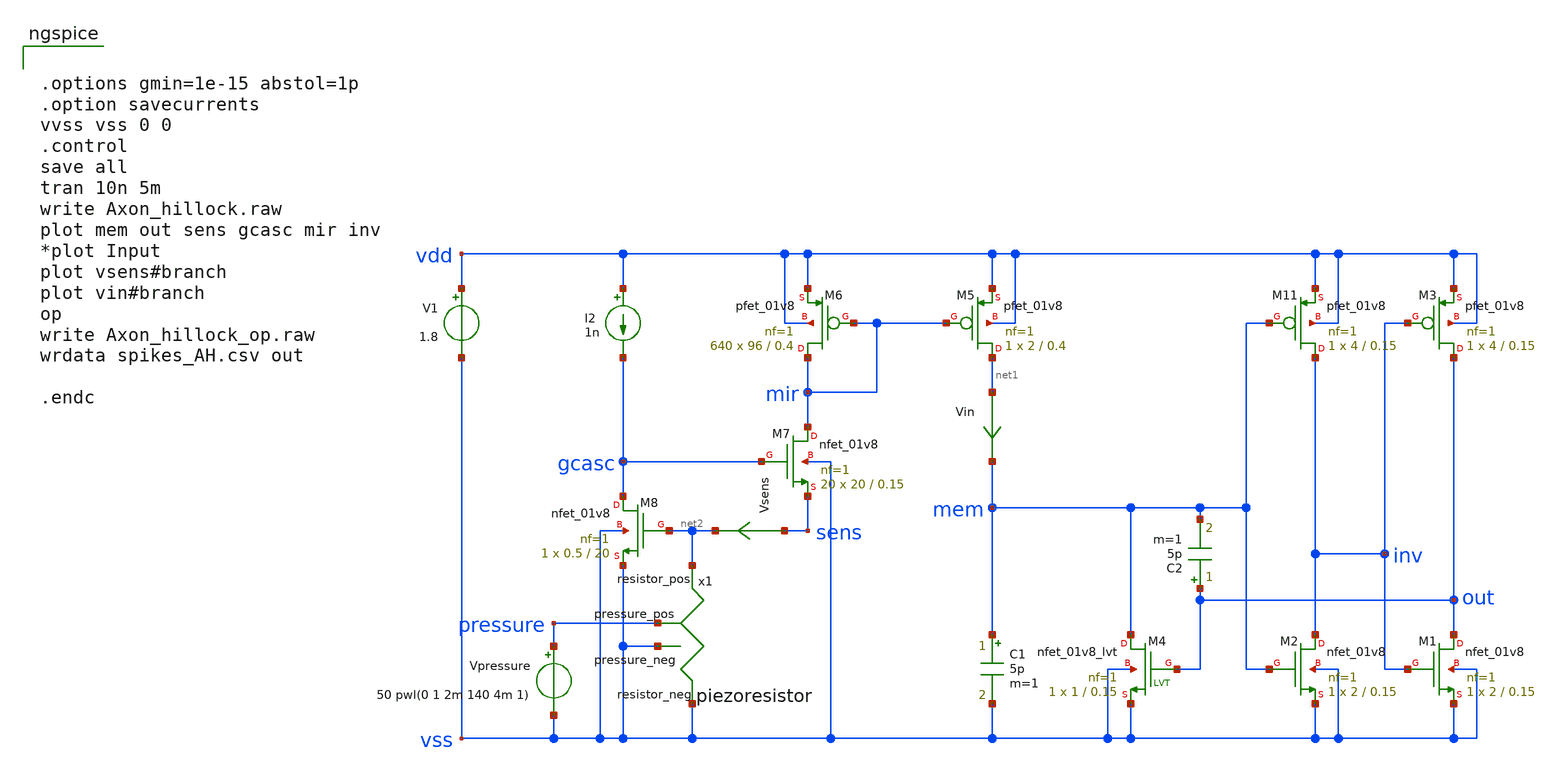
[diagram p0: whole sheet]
** sch_path: circuits/Axon_Hillock.sch
* Copyright 2020 Stefan Frederik Schippers
* Licensed under the Apache License, Version 2.0 (the "License");
* you may not use this file except in compliance with the License.
* You may obtain a copy of the License at
* https://www.apache.org/licenses/LICENSE-2.0
* Unless required by applicable law or agreed to in writing, software
* distributed under the License is distributed on an "AS IS" BASIS,
* WITHOUT WARRANTIES OR CONDITIONS OF ANY KIND, either express or implied.
* See the License for the specific language governing permissions and
* limitations under the License.
**.subckt Axon_Hillock
XM2 inv mem vss vss sky130_fd_pr__nfet_01v8 L=0.15 W=2 nf=1 ad='int((1 + 1)/2) * 2 / 1 * 0.29' as='int((1 + 2)/2) * 2 / 1 * 0.29'
+ pd='2*int((1 + 1)/2) * (2 / 1 + 0.29)' ps='2*int((1 + 2)/2) * (2 / 1 + 0.29)' nrd='0.29 / 2 ' nrs='0.29 / 2 '
+ sa=0 sb=0 sd=0 mult=1 m=1
XM11 inv mem vdd vdd sky130_fd_pr__pfet_01v8 L=0.15 W=4 nf=1 ad='int((nf+1)/2) * W/nf * 0.29' as='int((nf+2)/2) * W/nf * 0.29'
+ pd='2*int((nf+1)/2) * (W/nf + 0.29)' ps='2*int((nf+2)/2) * (W/nf + 0.29)' nrd='0.29 / W' nrs='0.29 / W'
+ sa=0 sb=0 sd=0 mult=1 m=1
XM1 out inv vss vss sky130_fd_pr__nfet_01v8 L=0.15 W=2 nf=1 ad='int((1 + 1)/2) * 2 / 1 * 0.29' as='int((1 + 2)/2) * 2 / 1 * 0.29'
+ pd='2*int((1 + 1)/2) * (2 / 1 + 0.29)' ps='2*int((1 + 2)/2) * (2 / 1 + 0.29)' nrd='0.29 / 2 ' nrs='0.29 / 2 '
+ sa=0 sb=0 sd=0 mult=1 m=1
XM3 out inv vdd vdd sky130_fd_pr__pfet_01v8 L=0.15 W=4 nf=1 ad='int((nf+1)/2) * W/nf * 0.29' as='int((nf+2)/2) * W/nf * 0.29'
+ pd='2*int((nf+1)/2) * (W/nf + 0.29)' ps='2*int((nf+2)/2) * (W/nf + 0.29)' nrd='0.29 / W' nrs='0.29 / W'
+ sa=0 sb=0 sd=0 mult=1 m=1
C2 out mem 5p m=1
V1 vdd vss 1.8
I2 vdd gcasc 1n
C1 mem vss 5p m=1
Vsens sens net2 0
.save i(vsens)
XM5 net1 mir vdd vdd sky130_fd_pr__pfet_01v8 L=0.4 W=2 nf=1 ad='int((nf+1)/2) * W/nf * 0.29' as='int((nf+2)/2) * W/nf * 0.29'
+ pd='2*int((nf+1)/2) * (W/nf + 0.29)' ps='2*int((nf+2)/2) * (W/nf + 0.29)' nrd='0.29 / W' nrs='0.29 / W'
+ sa=0 sb=0 sd=0 mult=1 m=1
XM6 mir mir vdd vdd sky130_fd_pr__pfet_01v8 L=0.4 W=96 nf=1 ad='int((nf+1)/2) * W/nf * 0.29' as='int((nf+2)/2) * W/nf * 0.29'
+ pd='2*int((nf+1)/2) * (W/nf + 0.29)' ps='2*int((nf+2)/2) * (W/nf + 0.29)' nrd='0.29 / W' nrs='0.29 / W'
+ sa=0 sb=0 sd=0 mult=640 m=640
XM4 mem out vss vss sky130_fd_pr__nfet_01v8_lvt L=0.15 W=1 nf=1 ad='int((1 + 1)/2) * 1 / 1 * 0.29' as='int((1 + 2)/2) * 1 / 1 * 0.29'
+ pd='2*int((1 + 1)/2) * (1 / 1 + 0.29)' ps='2*int((1 + 2)/2) * (1 / 1 + 0.29)' nrd='0.29 / 1 ' nrs='0.29 / 1 '
+ sa=0 sb=0 sd=0 mult=1 m=1
XM7 mir gcasc sens vss sky130_fd_pr__nfet_01v8 L=0.15 W=20 nf=1 ad='int((1 + 1)/2) * 20 / 1 * 0.29' as='int((1 + 2)/2) * 20 / 1 * 0.29'
+ pd='2*int((1 + 1)/2) * (20 / 1 + 0.29)' ps='2*int((1 + 2)/2) * (20 / 1 + 0.29)' nrd='0.29 / 20 ' nrs='0.29 / 20 '
+ sa=0 sb=0 sd=0 mult=20 m=20
XM8 gcasc net2 vss vss sky130_fd_pr__nfet_01v8 L=20 W=0.5 nf=1 ad='int((1 + 1)/2) * 0.5 / 1 * 0.29' as='int((1 + 2)/2) * 0.5 / 1 * 0.29'
+ pd='2*int((1 + 1)/2) * (0.5 / 1 + 0.29)' ps='2*int((1 + 2)/2) * (0.5 / 1 + 0.29)' nrd='0.29 / 0.5 ' nrs='0.29 / 0.5 '
+ sa=0 sb=0 sd=0 mult=1 m=1
Vin net1 mem 0
.save i(vin)
x1 pressure vss net2 vss piezoresistor
Vpressure pressure vss 50 pwl(0 1 2m 140 4m 1)
**** begin user architecture code


.options gmin=1e-15 abstol=1p
.option savecurrents
vvss vss 0 0
.control
save all
tran 10n 5m
write Axon_hillock.raw
plot mem out sens gcasc mir inv
*plot Input
plot vsens#branch
plot vin#branch
op
write Axon_hillock_op.raw
wrdata spikes_AH.csv out

.endc


 .lib $::SKYWATER_MODELS/models/sky130.lib.spice tt

.param mc_mm_switch=0
.param mc_pr_switch=1


**** end user architecture code
**.ends

* expanding   symbol:  /home/cmaier/.xschem/sky130_TAC3/circuits/piezoresistor.sym # of pins=4
** sym_path: circuits/piezoresistor.sym
** sch_path: circuits/piezoresistor.sch
.subckt piezoresistor pressure_pos pressure_neg resistor_pos resistor_neg
*.ipin pressure_pos
*.ipin pressure_neg
*.iopin resistor_pos
*.iopin resistor_neg
Broot sqrtp 0 V = sqrt(v(pressure_pos,pressure_neg))
Bres res 0 V = 106*(50/v(sqrtp)-1)*exp(-0.328*v(sqrtp))+15
Brvar resistor_pos resistor_neg I = V(resistor_pos,resistor_neg)/V(res)
.ends

.end
